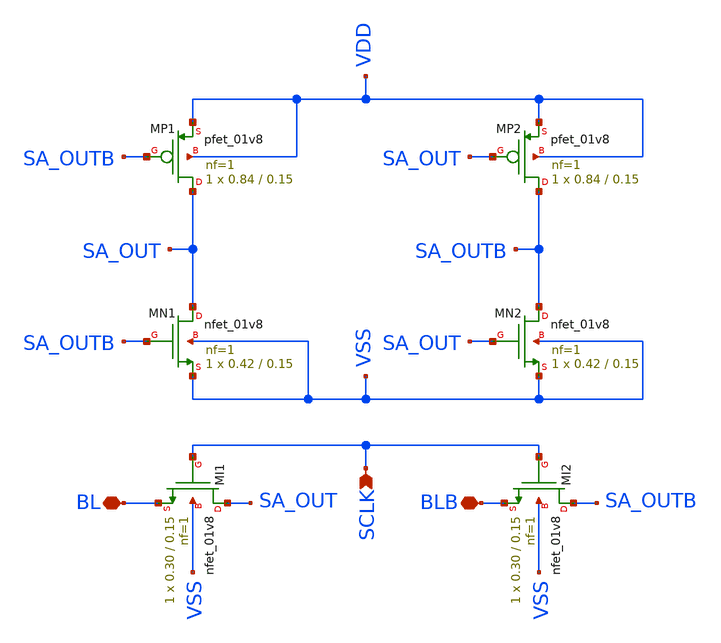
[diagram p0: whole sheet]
** sch_path: cells/sense_amp.sch
**.subckt sense_amp SCLK BL BLB
*.ipin SCLK
*.iopin BL
*.iopin BLB
XMP1 SA_OUT SA_OUTB VDD VDD sky130_fd_pr__pfet_01v8 L=0.15 W=0.84 nf=1 ad='int((nf+1)/2) * W/nf * 0.29'
+ as='int((nf+2)/2) * W/nf * 0.29' pd='2*int((nf+1)/2) * (W/nf + 0.29)' ps='2*int((nf+2)/2) * (W/nf + 0.29)'
+ nrd='0.29 / W' nrs='0.29 / W' sa=0 sb=0 sd=0 mult=1 m=1
XMP2 SA_OUTB SA_OUT VDD VDD sky130_fd_pr__pfet_01v8 L=0.15 W=0.84 nf=1 ad='int((nf+1)/2) * W/nf * 0.29'
+ as='int((nf+2)/2) * W/nf * 0.29' pd='2*int((nf+1)/2) * (W/nf + 0.29)' ps='2*int((nf+2)/2) * (W/nf + 0.29)'
+ nrd='0.29 / W' nrs='0.29 / W' sa=0 sb=0 sd=0 mult=1 m=1
XMN1 SA_OUT SA_OUTB VSS VSS sky130_fd_pr__nfet_01v8 L=0.15 W=0.42 nf=1 ad='int((1 + 1)/2) * 0.42 / 1 * 0.29'
+ as='int((1 + 2)/2) * 0.42 / 1 * 0.29' pd='2*int((1 + 1)/2) * (0.42 / 1 + 0.29)' ps='2*int((1 + 2)/2) * (0.42 / 1 + 0.29)'
+ nrd='0.29 / 0.42 ' nrs='0.29 / 0.42 ' sa=0 sb=0 sd=0 mult=1 m=1
XMN2 SA_OUTB SA_OUT VSS VSS sky130_fd_pr__nfet_01v8 L=0.15 W=0.42 nf=1 ad='int((1 + 1)/2) * 0.42 / 1 * 0.29'
+ as='int((1 + 2)/2) * 0.42 / 1 * 0.29' pd='2*int((1 + 1)/2) * (0.42 / 1 + 0.29)' ps='2*int((1 + 2)/2) * (0.42 / 1 + 0.29)'
+ nrd='0.29 / 0.42 ' nrs='0.29 / 0.42 ' sa=0 sb=0 sd=0 mult=1 m=1
XMI1 SA_OUT SCLK BL VSS sky130_fd_pr__nfet_01v8 L=0.15 W=0.30 nf=1 ad='int((1 + 1)/2) * 0.30 / 1 * 0.29'
+ as='int((1 + 2)/2) * 0.30 / 1 * 0.29' pd='2*int((1 + 1)/2) * (0.30 / 1 + 0.29)' ps='2*int((1 + 2)/2) * (0.30 / 1 + 0.29)'
+ nrd='0.29 / 0.30 ' nrs='0.29 / 0.30 ' sa=0 sb=0 sd=0 mult=1 m=1
XMI2 SA_OUTB SCLK BLB VSS sky130_fd_pr__nfet_01v8 L=0.15 W=0.30 nf=1 ad='int((1 + 1)/2) * 0.30 / 1 * 0.29'
+ as='int((1 + 2)/2) * 0.30 / 1 * 0.29' pd='2*int((1 + 1)/2) * (0.30 / 1 + 0.29)' ps='2*int((1 + 2)/2) * (0.30 / 1 + 0.29)'
+ nrd='0.29 / 0.30 ' nrs='0.29 / 0.30 ' sa=0 sb=0 sd=0 mult=1 m=1
**.ends
.end
